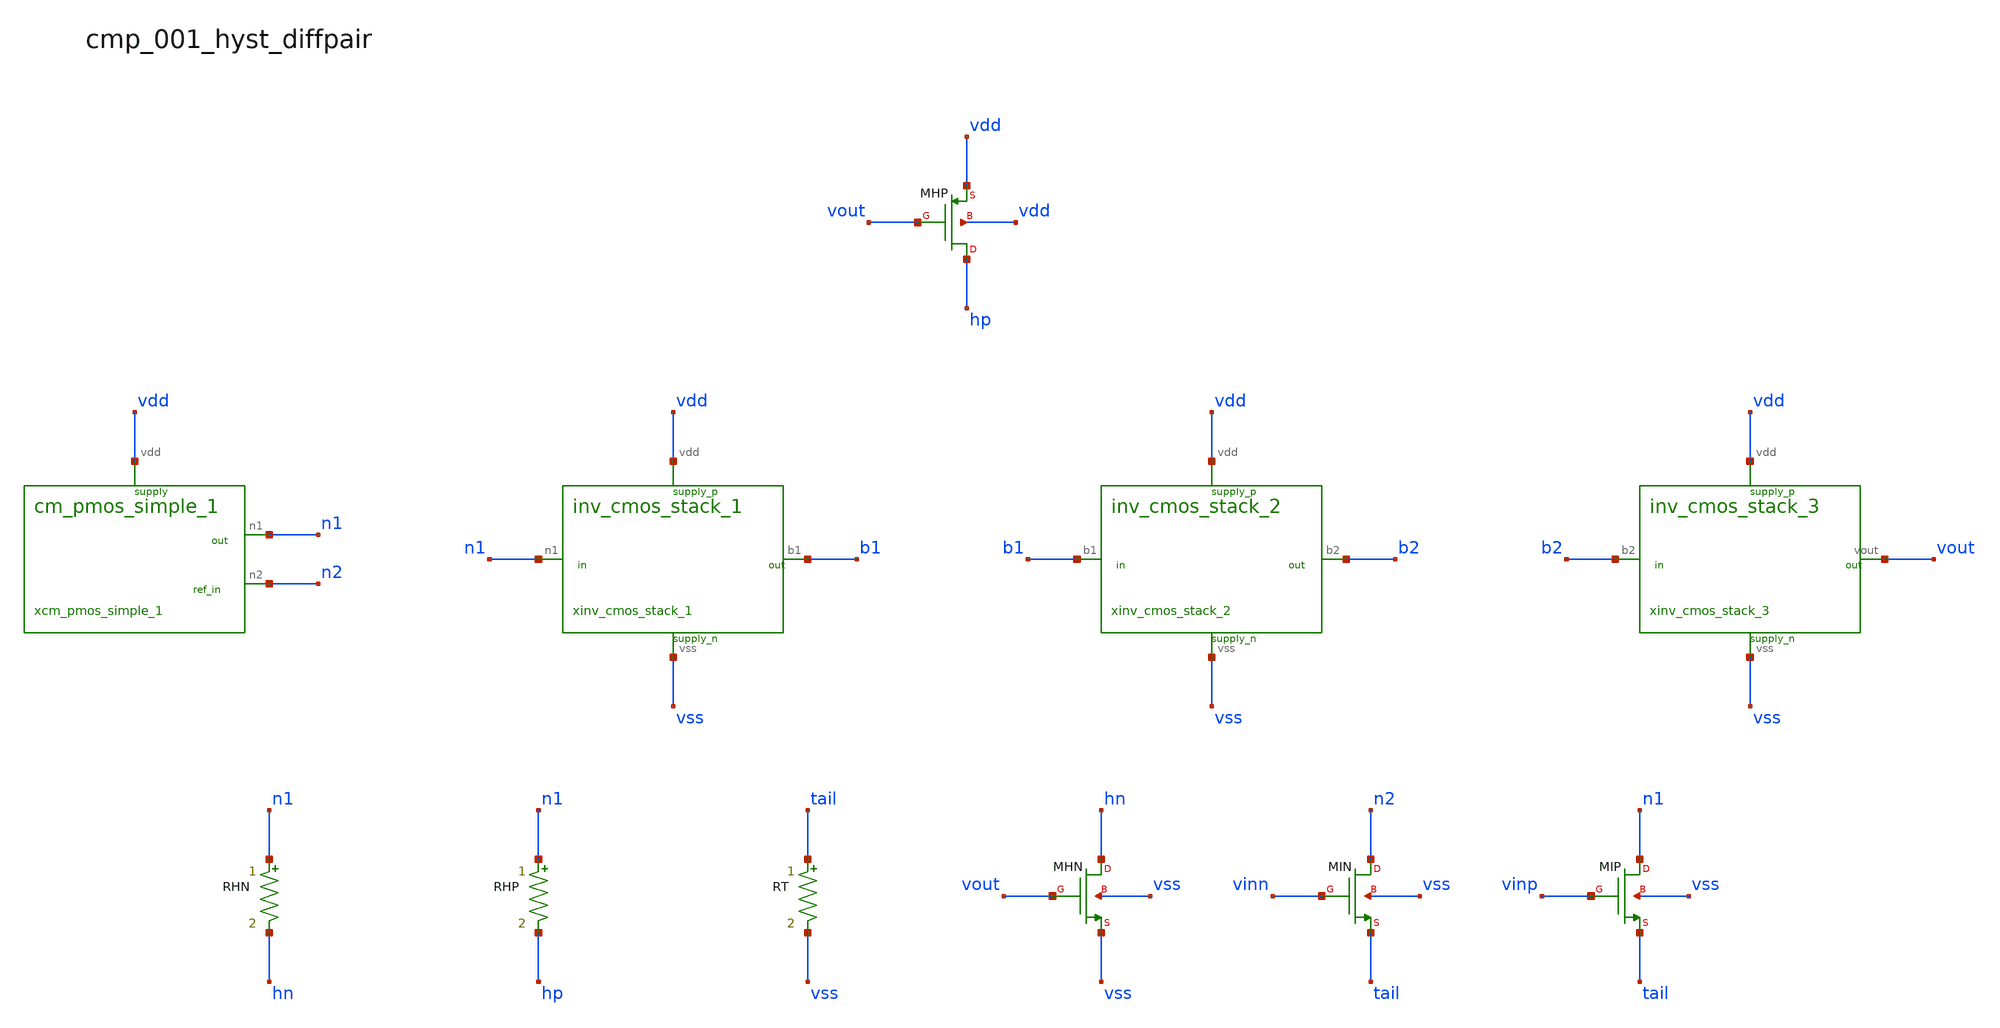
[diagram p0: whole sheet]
** sch_path: analog-db/raw/cmp_001_hyst_diffpair/hier/cmp_001_hyst_diffpair.sch
**.subckt cmp_001_hyst_diffpair
xcm_pmos_simple_1 n1 n2 vdd cm_pmos_simple_1
xinv_cmos_stack_1 n1 b1 vdd vss inv_cmos_stack_1
xinv_cmos_stack_2 b1 b2 vdd vss inv_cmos_stack_2
xinv_cmos_stack_3 b2 vout vdd vss inv_cmos_stack_3
RHN n1 hn x_dut_rhn_value m=1
RHP n1 hp x_dut_rhp_value m=1
RT tail vss x_rtail m=1
XMHN hn vout vss vss sg13_lv_nmos w=x_dut_xmhn_w l=x_dut_xmhn_l ng=1 m=x_dut_xmhn_m
XMHP hp vout vdd vdd sg13_lv_pmos w=x_dut_xmhp_w l=x_dut_xmhp_l ng=1 m=x_dut_xmhp_m
XMIN n2 vinn tail vss sg13_lv_nmos w=x_dut_xmin_w l=x_dut_xmin_l ng=1 m=x_dut_xmin_m
XMIP n1 vinp tail vss sg13_lv_nmos w=x_dut_xmip_w l=x_dut_xmip_l ng=1 m=x_dut_xmip_m
**.ends

* expanding   symbol:  blocks/cm_pmos_simple_1.sym # of pins=3
** sym_path: analog-db/raw/cmp_001_hyst_diffpair/hier/blocks/cm_pmos_simple_1.sym
** sch_path: analog-db/raw/cmp_001_hyst_diffpair/hier/blocks/cm_pmos_simple_1.sch
.subckt cm_pmos_simple_1 n1 n2 vdd
*.iopin vdd
*.opin n2
*.opin n1
XMPLD n2 n2 vdd vdd sg13_lv_pmos w=x_dut_xmpld_w l=x_dut_xmpld_l ng=1 m=x_dut_xmpld_m
XMPLM n1 n2 vdd vdd sg13_lv_pmos w=x_dut_xmplm_w l=x_dut_xmplm_l ng=1 m=x_dut_xmplm_m
.ends


* expanding   symbol:  blocks/inv_cmos_stack_1.sym # of pins=4
** sym_path: analog-db/raw/cmp_001_hyst_diffpair/hier/blocks/inv_cmos_stack_1.sym
** sch_path: analog-db/raw/cmp_001_hyst_diffpair/hier/blocks/inv_cmos_stack_1.sch
.subckt inv_cmos_stack_1 n1 b1 vdd vss
*.ipin n1
*.iopin vdd
*.iopin vss
*.opin b1
XMB1N b1 n1 vss vss sg13_lv_nmos w=x_dut_xmb1n_w l=x_dut_xmb1n_l ng=1 m=x_dut_xmb1n_m
XMB1P b1 n1 vdd vdd sg13_lv_pmos w=x_dut_xmb1p_w l=x_dut_xmb1p_l ng=1 m=x_dut_xmb1p_m
.ends


* expanding   symbol:  blocks/inv_cmos_stack_2.sym # of pins=4
** sym_path: analog-db/raw/cmp_001_hyst_diffpair/hier/blocks/inv_cmos_stack_2.sym
** sch_path: analog-db/raw/cmp_001_hyst_diffpair/hier/blocks/inv_cmos_stack_2.sch
.subckt inv_cmos_stack_2 b1 b2 vdd vss
*.ipin b1
*.iopin vdd
*.iopin vss
*.opin b2
XMB2N b2 b1 vss vss sg13_lv_nmos w=x_dut_xmb2n_w l=x_dut_xmb2n_l ng=1 m=x_dut_xmb2n_m
XMB2P b2 b1 vdd vdd sg13_lv_pmos w=x_dut_xmb2p_w l=x_dut_xmb2p_l ng=1 m=x_dut_xmb2p_m
.ends


* expanding   symbol:  blocks/inv_cmos_stack_3.sym # of pins=4
** sym_path: analog-db/raw/cmp_001_hyst_diffpair/hier/blocks/inv_cmos_stack_3.sym
** sch_path: analog-db/raw/cmp_001_hyst_diffpair/hier/blocks/inv_cmos_stack_3.sch
.subckt inv_cmos_stack_3 b2 vout vdd vss
*.ipin b2
*.iopin vdd
*.iopin vss
*.opin vout
XMB3N vout b2 vss vss sg13_lv_nmos w=x_dut_xmb3n_w l=x_dut_xmb3n_l ng=1 m=x_dut_xmb3n_m
XMB3P vout b2 vdd vdd sg13_lv_pmos w=x_dut_xmb3p_w l=x_dut_xmb3p_l ng=1 m=x_dut_xmb3p_m
.ends

.end
